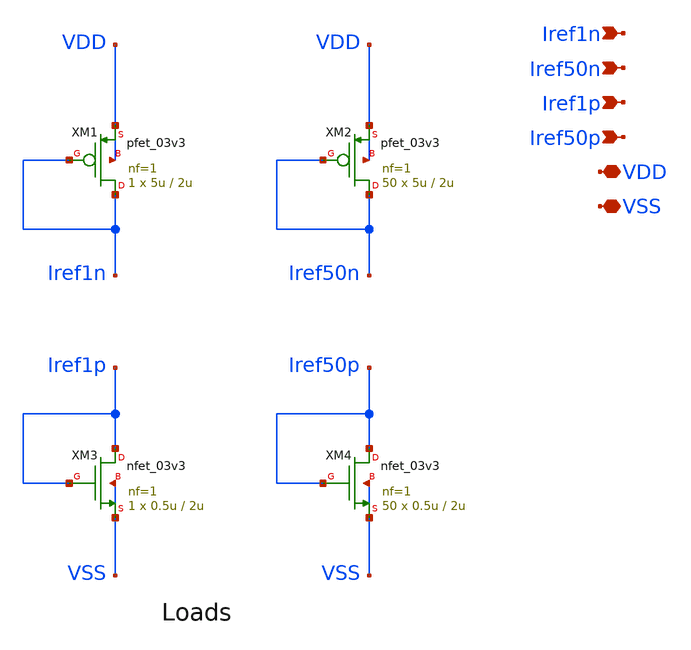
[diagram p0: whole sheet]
** sch_path: designs/current_reference_load/xschem/current_reference_load.sch
**.subckt current_reference_load Iref1n VDD VSS Iref50n Iref1p Iref50p
*.ipin Iref1n
*.iopin VDD
*.iopin VSS
*.ipin Iref50n
*.ipin Iref1p
*.ipin Iref50p
XM1 Iref1n Iref1n VDD VDD pfet_03v3 L=2u W=5u nf=1 ad='int((nf+1)/2) * W/nf * 0.18u' as='int((nf+2)/2) * W/nf * 0.18u'
+ pd='2*int((nf+1)/2) * (W/nf + 0.18u)' ps='2*int((nf+2)/2) * (W/nf + 0.18u)' nrd='0.18u / W' nrs='0.18u / W'
+ sa=0 sb=0 sd=0 m=1
XM3 Iref1p Iref1p VSS VSS nfet_03v3 L=2u W=0.5u nf=1 ad='int((nf+1)/2) * W/nf * 0.18u' as='int((nf+2)/2) * W/nf * 0.18u'
+ pd='2*int((nf+1)/2) * (W/nf + 0.18u)' ps='2*int((nf+2)/2) * (W/nf + 0.18u)' nrd='0.18u / W' nrs='0.18u / W'
+ sa=0 sb=0 sd=0 m=1
XM2 Iref50n Iref50n VDD VDD pfet_03v3 L=2u W=5u nf=1 ad='int((nf+1)/2) * W/nf * 0.18u' as='int((nf+2)/2) * W/nf * 0.18u'
+ pd='2*int((nf+1)/2) * (W/nf + 0.18u)' ps='2*int((nf+2)/2) * (W/nf + 0.18u)' nrd='0.18u / W' nrs='0.18u / W'
+ sa=0 sb=0 sd=0 m=50
XM4 Iref50p Iref50p VSS VSS nfet_03v3 L=2u W=0.5u nf=1 ad='int((nf+1)/2) * W/nf * 0.18u' as='int((nf+2)/2) * W/nf * 0.18u'
+ pd='2*int((nf+1)/2) * (W/nf + 0.18u)' ps='2*int((nf+2)/2) * (W/nf + 0.18u)' nrd='0.18u / W' nrs='0.18u / W'
+ sa=0 sb=0 sd=0 m=50
**.ends
.end
